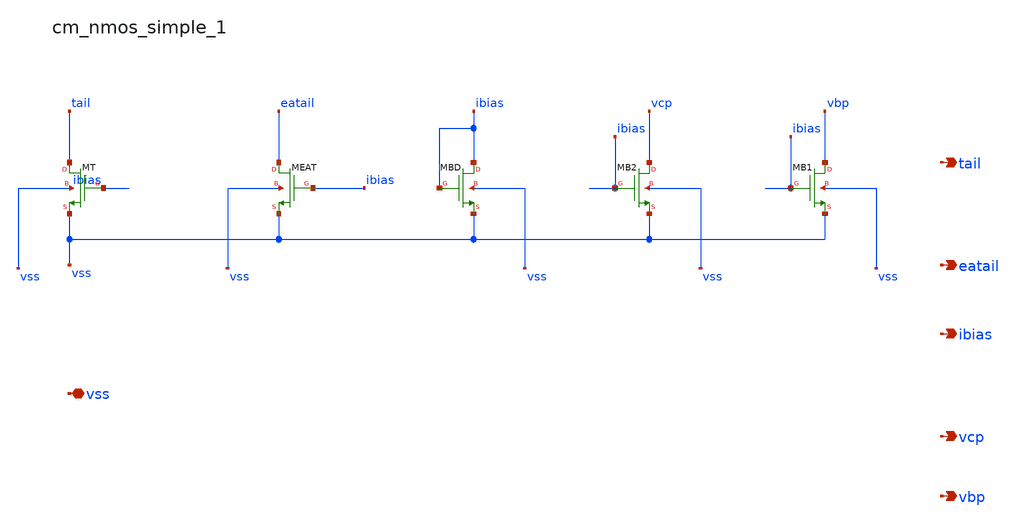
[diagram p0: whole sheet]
** sch_path: analog-db/raw/amp_023_fer_fd2s/hier/blocks/cm_nmos_simple_1.sch
**.subckt cm_nmos_simple_1 vss tail eatail ibias vcp vbp
*.iopin vss
*.opin tail
*.opin eatail
*.opin ibias
*.opin vcp
*.opin vbp
XMB1 vbp ibias vss vss sg13_lv_nmos w=x_dut_xmb1_w l=x_dut_xmb1_l ng=1 m=x_dut_xmb1_m
XMB2 vcp ibias vss vss sg13_lv_nmos w=x_dut_xmb2_w l=x_dut_xmb2_l ng=1 m=x_dut_xmb2_m
XMBD ibias ibias vss vss sg13_lv_nmos w=x_dut_xmbd_w l=x_dut_xmbd_l ng=1 m=x_dut_xmbd_m
XMEAT eatail ibias vss vss sg13_lv_nmos w=x_dut_xmeat_w l=x_dut_xmeat_l ng=1 m=x_dut_xmeat_m
XMT tail ibias vss vss sg13_lv_nmos w=x_dut_xmt_w l=x_dut_xmt_l ng=1 m=x_dut_xmt_m
**.ends
.end
